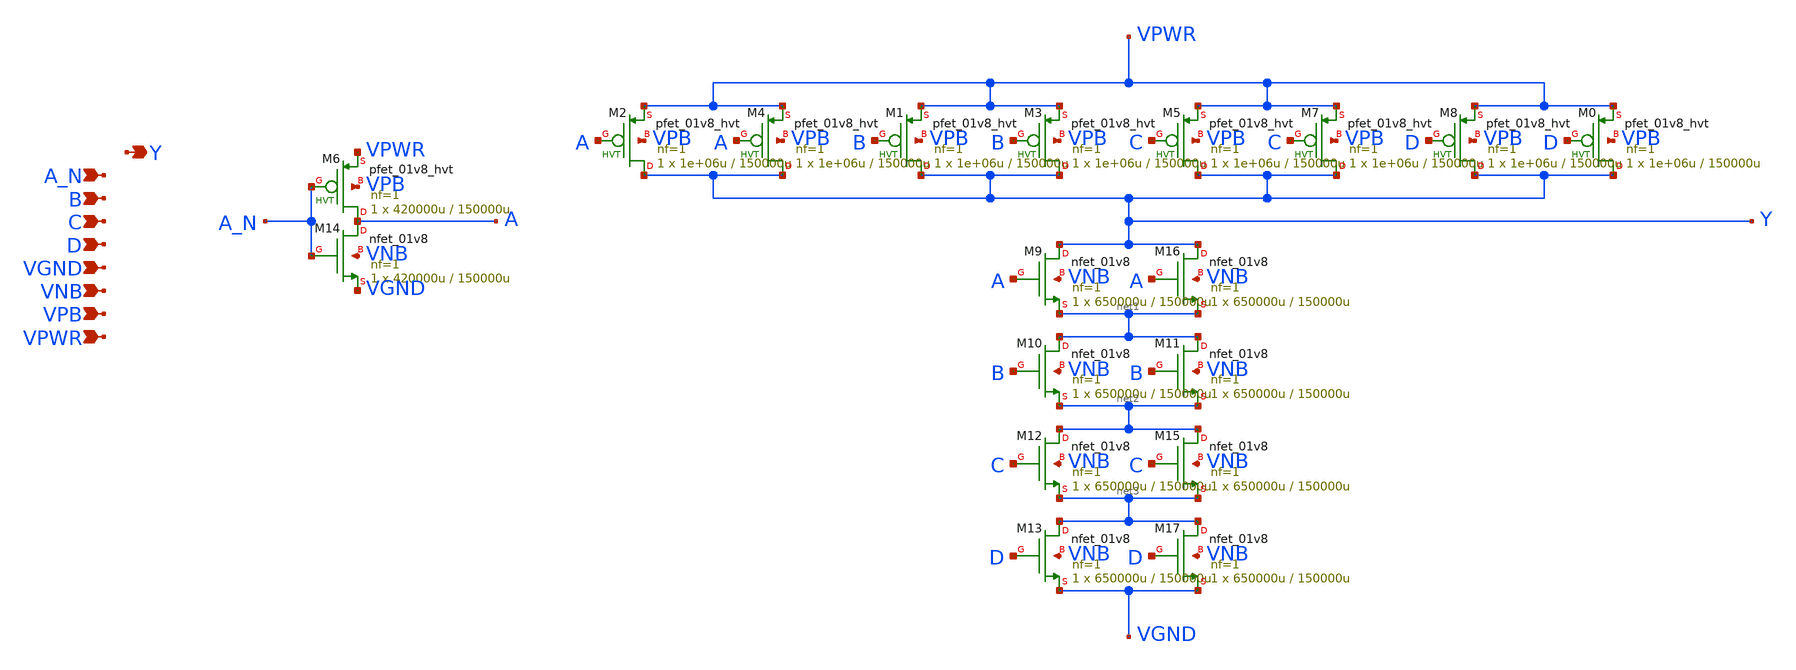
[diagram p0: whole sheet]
** sch_path: schematics/nand4b/sky130_fd_sc_hd__nand4b_2.sch
**.subckt sky130_fd_sc_hd__nand4b_2 A_N B C D VGND VNB VPB VPWR Y
*.ipin A_N
*.ipin B
*.ipin C
*.ipin D
*.ipin VGND
*.ipin VNB
*.ipin VPB
*.ipin VPWR
*.opin Y
XM0 Y D VPWR VPB sky130_fd_pr__pfet_01v8_hvt L=150000u W=1e+06u nf=1 ad='int((1 + 1)/2) * 1e+06u / 1 * 0.29'
+ as='int((1 + 2)/2) * 1e+06u / 1 * 0.29' pd='2*int((1 + 1)/2) * (1e+06u / 1 + 0.29)' ps='2*int((1 + 2)/2) * (1e+06u / 1 + 0.29)'
+ nrd='0.29 / 1e+06u ' nrs='0.29 / 1e+06u ' sa=0 sb=0 sd=0 mult=1 m=1
XM1 Y B VPWR VPB sky130_fd_pr__pfet_01v8_hvt L=150000u W=1e+06u nf=1 ad='int((1 + 1)/2) * 1e+06u / 1 * 0.29'
+ as='int((1 + 2)/2) * 1e+06u / 1 * 0.29' pd='2*int((1 + 1)/2) * (1e+06u / 1 + 0.29)' ps='2*int((1 + 2)/2) * (1e+06u / 1 + 0.29)'
+ nrd='0.29 / 1e+06u ' nrs='0.29 / 1e+06u ' sa=0 sb=0 sd=0 mult=1 m=1
XM2 Y A VPWR VPB sky130_fd_pr__pfet_01v8_hvt L=150000u W=1e+06u nf=1 ad='int((1 + 1)/2) * 1e+06u / 1 * 0.29'
+ as='int((1 + 2)/2) * 1e+06u / 1 * 0.29' pd='2*int((1 + 1)/2) * (1e+06u / 1 + 0.29)' ps='2*int((1 + 2)/2) * (1e+06u / 1 + 0.29)'
+ nrd='0.29 / 1e+06u ' nrs='0.29 / 1e+06u ' sa=0 sb=0 sd=0 mult=1 m=1
XM3 Y B VPWR VPB sky130_fd_pr__pfet_01v8_hvt L=150000u W=1e+06u nf=1 ad='int((1 + 1)/2) * 1e+06u / 1 * 0.29'
+ as='int((1 + 2)/2) * 1e+06u / 1 * 0.29' pd='2*int((1 + 1)/2) * (1e+06u / 1 + 0.29)' ps='2*int((1 + 2)/2) * (1e+06u / 1 + 0.29)'
+ nrd='0.29 / 1e+06u ' nrs='0.29 / 1e+06u ' sa=0 sb=0 sd=0 mult=1 m=1
XM4 Y A VPWR VPB sky130_fd_pr__pfet_01v8_hvt L=150000u W=1e+06u nf=1 ad='int((1 + 1)/2) * 1e+06u / 1 * 0.29'
+ as='int((1 + 2)/2) * 1e+06u / 1 * 0.29' pd='2*int((1 + 1)/2) * (1e+06u / 1 + 0.29)' ps='2*int((1 + 2)/2) * (1e+06u / 1 + 0.29)'
+ nrd='0.29 / 1e+06u ' nrs='0.29 / 1e+06u ' sa=0 sb=0 sd=0 mult=1 m=1
XM5 Y C VPWR VPB sky130_fd_pr__pfet_01v8_hvt L=150000u W=1e+06u nf=1 ad='int((1 + 1)/2) * 1e+06u / 1 * 0.29'
+ as='int((1 + 2)/2) * 1e+06u / 1 * 0.29' pd='2*int((1 + 1)/2) * (1e+06u / 1 + 0.29)' ps='2*int((1 + 2)/2) * (1e+06u / 1 + 0.29)'
+ nrd='0.29 / 1e+06u ' nrs='0.29 / 1e+06u ' sa=0 sb=0 sd=0 mult=1 m=1
XM6 A A_N VPWR VPB sky130_fd_pr__pfet_01v8_hvt L=150000u W=420000u nf=1 ad='int((1 + 1)/2) * 420000u / 1 * 0.29'
+ as='int((1 + 2)/2) * 420000u / 1 * 0.29' pd='2*int((1 + 1)/2) * (420000u / 1 + 0.29)' ps='2*int((1 + 2)/2) * (420000u / 1 + 0.29)'
+ nrd='0.29 / 420000u ' nrs='0.29 / 420000u ' sa=0 sb=0 sd=0 mult=1 m=1
XM7 Y C VPWR VPB sky130_fd_pr__pfet_01v8_hvt L=150000u W=1e+06u nf=1 ad='int((1 + 1)/2) * 1e+06u / 1 * 0.29'
+ as='int((1 + 2)/2) * 1e+06u / 1 * 0.29' pd='2*int((1 + 1)/2) * (1e+06u / 1 + 0.29)' ps='2*int((1 + 2)/2) * (1e+06u / 1 + 0.29)'
+ nrd='0.29 / 1e+06u ' nrs='0.29 / 1e+06u ' sa=0 sb=0 sd=0 mult=1 m=1
XM8 Y D VPWR VPB sky130_fd_pr__pfet_01v8_hvt L=150000u W=1e+06u nf=1 ad='int((1 + 1)/2) * 1e+06u / 1 * 0.29'
+ as='int((1 + 2)/2) * 1e+06u / 1 * 0.29' pd='2*int((1 + 1)/2) * (1e+06u / 1 + 0.29)' ps='2*int((1 + 2)/2) * (1e+06u / 1 + 0.29)'
+ nrd='0.29 / 1e+06u ' nrs='0.29 / 1e+06u ' sa=0 sb=0 sd=0 mult=1 m=1
XM9 Y A net1 VNB sky130_fd_pr__nfet_01v8 L=150000u W=650000u nf=1 ad='int((1 + 1)/2) * 650000u / 1 * 0.29'
+ as='int((1 + 2)/2) * 650000u / 1 * 0.29' pd='2*int((1 + 1)/2) * (650000u / 1 + 0.29)' ps='2*int((1 + 2)/2) * (650000u / 1 + 0.29)'
+ nrd='0.29 / 650000u ' nrs='0.29 / 650000u ' sa=0 sb=0 sd=0 mult=1 m=1
XM10 net1 B net2 VNB sky130_fd_pr__nfet_01v8 L=150000u W=650000u nf=1 ad='int((1 + 1)/2) * 650000u / 1 * 0.29'
+ as='int((1 + 2)/2) * 650000u / 1 * 0.29' pd='2*int((1 + 1)/2) * (650000u / 1 + 0.29)' ps='2*int((1 + 2)/2) * (650000u / 1 + 0.29)'
+ nrd='0.29 / 650000u ' nrs='0.29 / 650000u ' sa=0 sb=0 sd=0 mult=1 m=1
XM11 net1 B net2 VNB sky130_fd_pr__nfet_01v8 L=150000u W=650000u nf=1 ad='int((1 + 1)/2) * 650000u / 1 * 0.29'
+ as='int((1 + 2)/2) * 650000u / 1 * 0.29' pd='2*int((1 + 1)/2) * (650000u / 1 + 0.29)' ps='2*int((1 + 2)/2) * (650000u / 1 + 0.29)'
+ nrd='0.29 / 650000u ' nrs='0.29 / 650000u ' sa=0 sb=0 sd=0 mult=1 m=1
XM12 net2 C net3 VNB sky130_fd_pr__nfet_01v8 L=150000u W=650000u nf=1 ad='int((1 + 1)/2) * 650000u / 1 * 0.29'
+ as='int((1 + 2)/2) * 650000u / 1 * 0.29' pd='2*int((1 + 1)/2) * (650000u / 1 + 0.29)' ps='2*int((1 + 2)/2) * (650000u / 1 + 0.29)'
+ nrd='0.29 / 650000u ' nrs='0.29 / 650000u ' sa=0 sb=0 sd=0 mult=1 m=1
XM13 net3 D VGND VNB sky130_fd_pr__nfet_01v8 L=150000u W=650000u nf=1 ad='int((1 + 1)/2) * 650000u / 1 * 0.29'
+ as='int((1 + 2)/2) * 650000u / 1 * 0.29' pd='2*int((1 + 1)/2) * (650000u / 1 + 0.29)' ps='2*int((1 + 2)/2) * (650000u / 1 + 0.29)'
+ nrd='0.29 / 650000u ' nrs='0.29 / 650000u ' sa=0 sb=0 sd=0 mult=1 m=1
XM14 A A_N VGND VNB sky130_fd_pr__nfet_01v8 L=150000u W=420000u nf=1 ad='int((1 + 1)/2) * 420000u / 1 * 0.29'
+ as='int((1 + 2)/2) * 420000u / 1 * 0.29' pd='2*int((1 + 1)/2) * (420000u / 1 + 0.29)' ps='2*int((1 + 2)/2) * (420000u / 1 + 0.29)'
+ nrd='0.29 / 420000u ' nrs='0.29 / 420000u ' sa=0 sb=0 sd=0 mult=1 m=1
XM15 net2 C net3 VNB sky130_fd_pr__nfet_01v8 L=150000u W=650000u nf=1 ad='int((1 + 1)/2) * 650000u / 1 * 0.29'
+ as='int((1 + 2)/2) * 650000u / 1 * 0.29' pd='2*int((1 + 1)/2) * (650000u / 1 + 0.29)' ps='2*int((1 + 2)/2) * (650000u / 1 + 0.29)'
+ nrd='0.29 / 650000u ' nrs='0.29 / 650000u ' sa=0 sb=0 sd=0 mult=1 m=1
XM16 Y A net1 VNB sky130_fd_pr__nfet_01v8 L=150000u W=650000u nf=1 ad='int((1 + 1)/2) * 650000u / 1 * 0.29'
+ as='int((1 + 2)/2) * 650000u / 1 * 0.29' pd='2*int((1 + 1)/2) * (650000u / 1 + 0.29)' ps='2*int((1 + 2)/2) * (650000u / 1 + 0.29)'
+ nrd='0.29 / 650000u ' nrs='0.29 / 650000u ' sa=0 sb=0 sd=0 mult=1 m=1
XM17 net3 D VGND VNB sky130_fd_pr__nfet_01v8 L=150000u W=650000u nf=1 ad='int((1 + 1)/2) * 650000u / 1 * 0.29'
+ as='int((1 + 2)/2) * 650000u / 1 * 0.29' pd='2*int((1 + 1)/2) * (650000u / 1 + 0.29)' ps='2*int((1 + 2)/2) * (650000u / 1 + 0.29)'
+ nrd='0.29 / 650000u ' nrs='0.29 / 650000u ' sa=0 sb=0 sd=0 mult=1 m=1
**.ends
.end
